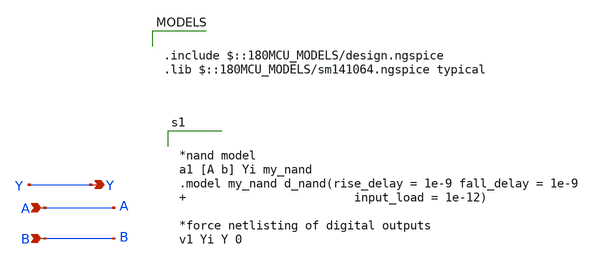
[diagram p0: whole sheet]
** sch_path: XSCHEM Files/nand.sch
**.subckt nand A Y B
*.ipin A
*.opin Y
*.ipin B
**** begin user architecture code


*nand model
a1 [A b] Yi my_nand
.model my_nand d_nand(rise_delay = 1e-9 fall_delay = 1e-9                         input_load =
+ 1e-12)

*force netlisting of digital outputs
v1 Yi Y 0



.include $::180MCU_MODELS/design.ngspice
.lib $::180MCU_MODELS/sm141064.ngspice typical

**** end user architecture code
**.ends
.end
